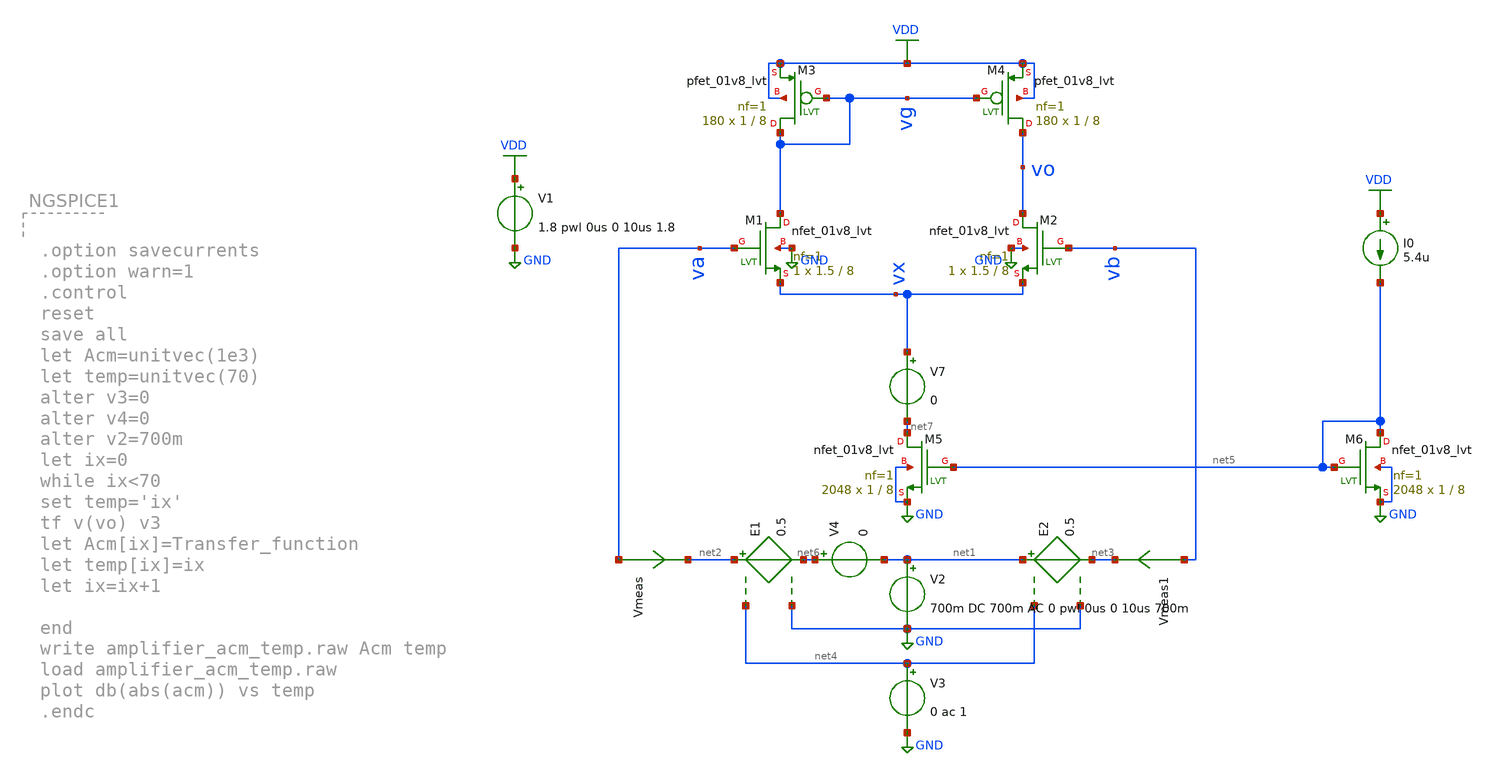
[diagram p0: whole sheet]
** sch_path: schematics/amplifier.sch
**.subckt amplifier
V1 VDD GND 1.8 pwl 0us 0 10us 1.8
V2 net1 GND 700m DC 700m AC 0 pwl 0us 0 10us 700m
Vmeas va net2 0
.save i(vmeas)
Vmeas1 vb net3 0
.save i(vmeas1)
XM2 vo vb vx GND sky130_fd_pr__nfet_01v8_lvt L=8 W=1.5 nf=1 ad='int((nf+1)/2) * W/nf * 0.29' as='int((nf+2)/2) * W/nf * 0.29'
+ pd='2*int((nf+1)/2) * (W/nf + 0.29)' ps='2*int((nf+2)/2) * (W/nf + 0.29)' nrd='0.29 / W' nrs='0.29 / W'
+ sa=0 sb=0 sd=0 mult=1 m=1
E1 net2 net6 net4 GND 0.5
E2 net1 net3 net4 GND 0.5
V3 net4 GND 0 ac 1
XM5 net7 net5 GND GND sky130_fd_pr__nfet_01v8_lvt L=8 W=1 nf=1 ad='int((nf+1)/2) * W/nf * 0.29' as='int((nf+2)/2) * W/nf * 0.29'
+ pd='2*int((nf+1)/2) * (W/nf + 0.29)' ps='2*int((nf+2)/2) * (W/nf + 0.29)' nrd='0.29 / W' nrs='0.29 / W'
+ sa=0 sb=0 sd=0 mult=2048 m=2048
XM6 net5 net5 GND GND sky130_fd_pr__nfet_01v8_lvt L=8 W=1 nf=1 ad='int((nf+1)/2) * W/nf * 0.29' as='int((nf+2)/2) * W/nf * 0.29'
+ pd='2*int((nf+1)/2) * (W/nf + 0.29)' ps='2*int((nf+2)/2) * (W/nf + 0.29)' nrd='0.29 / W' nrs='0.29 / W'
+ sa=0 sb=0 sd=0 mult=2048 m=2048
V4 net6 net1 0
XM1 vg va vx GND sky130_fd_pr__nfet_01v8_lvt L=8 W=1.5 nf=1 ad='int((nf+1)/2) * W/nf * 0.29' as='int((nf+2)/2) * W/nf * 0.29'
+ pd='2*int((nf+1)/2) * (W/nf + 0.29)' ps='2*int((nf+2)/2) * (W/nf + 0.29)' nrd='0.29 / W' nrs='0.29 / W'
+ sa=0 sb=0 sd=0 mult=1 m=1
XM3 vg vg VDD VDD sky130_fd_pr__pfet_01v8_lvt L=8 W=1 nf=1 ad='int((nf+1)/2) * W/nf * 0.29' as='int((nf+2)/2) * W/nf * 0.29'
+ pd='2*int((nf+1)/2) * (W/nf + 0.29)' ps='2*int((nf+2)/2) * (W/nf + 0.29)' nrd='0.29 / W' nrs='0.29 / W'
+ sa=0 sb=0 sd=0 mult=180 m=180
XM4 vo vg VDD VDD sky130_fd_pr__pfet_01v8_lvt L=8 W=1 nf=1 ad='int((nf+1)/2) * W/nf * 0.29' as='int((nf+2)/2) * W/nf * 0.29'
+ pd='2*int((nf+1)/2) * (W/nf + 0.29)' ps='2*int((nf+2)/2) * (W/nf + 0.29)' nrd='0.29 / W' nrs='0.29 / W'
+ sa=0 sb=0 sd=0 mult=180 m=180
V7 vx net7 0
I0 VDD net5 5.4u
**** begin user architecture code


.option savecurrents
.option warn=1

.control

save all   @m.xm1.msky130_fd_pr__nfet_01v8_lvt[id]  @m.xm2.msky130_fd_pr__nfet_01v8_lvt[id]
let Adm=unitvec(1e3)
let Vcm=unitvec(1e3)
let id1=unitvec(1e3)
let id2=unitvec(1e3)
let ix=0
alter v3=0
alter v4=0
while ix<1e3
let vcmtemp=ix/1e3
alter v2=vcmtemp
tf v(vo) v3
let Adm[ix]=Transfer_function
let Vcm[ix]=vcmtemp
let ix=ix+1
end
write amplifier_adm_vs_vcm.raw Adm Vcm
load amplifier_adm_vs_vcm.raw
plot (abs(adm)) vs vcm

op
let gm4=@m.xm4.msky130_fd_pr__pfet_01v8['gm']
let gm2=@m.xm2.msky130_fd_pr__nfet_01v8['gm']
let ib=@i0[current]
let irhs=@m.xm2.msky130_fd_pr__nfet_01v8['id']
let ilhs=@m.xm1.msky130_fd_pr__nfet_01v8['id']
let vthp=@m.xm3.msky130_fd_pr__pfet_01v8['vth']
let vthn=@m.xm1.msky130_fd_pr__nfet_01v8['vth']
print gm2 gm4
print irhs ilhs
let K=10^(-3.89062)
echo 'saturation cond. for M1 & M2 (by symmetry)'
echo 'is'
print vo - vx
echo 'greater than'
print vb - vx - vthn
echo 'saturation cond. for M3 & M4 (by symmetry)'
echo 'is'
print vdd - vo
echo 'greater than'
print vdd - vg - vthp
echo 'saturation cond. check w/ vo'
echo 'is'
print vo
echo 'between'
print vg + vthp
echo 'and'
print vb - vthn
echo 'common mode input sweep'
dc v2 -1.8 1.8 0.1
let vic=(va+vb)/2
let irhs=@m.xm2.msky130_fd_pr__nfet_01v8['id']
let ilhs=@m.xm1.msky130_fd_pr__nfet_01v8['id']
plot irhs ilhs ilhs/irhs
echo 'ac analysis'
ac dec 100 1 100e9
let vid=net2-net3
let irhs=@m.xm2.msky130_fd_pr__nfet_01v8['id']
let ilhs=@m.xm1.msky130_fd_pr__nfet_01v8['id']
plot db(abs(vo/vid))
echo 'dc gain (dB)'
print db(abs(vo/vid))[0]

dc i0 10u 100u 5u

.endc



.include $::SKYWATER_MODELS/cells/nfet_01v8/sky130_fd_pr__nfet_01v8__tt.corner.spice
.include $::SKYWATER_MODELS/cells/nfet_01v8_lvt/sky130_fd_pr__nfet_01v8_lvt__tt.corner.spice
.include $::SKYWATER_MODELS/cells/pfet_01v8/sky130_fd_pr__pfet_01v8__tt.corner.spice
.include $::SKYWATER_MODELS/cells/nfet_03v3_nvt/sky130_fd_pr__nfet_03v3_nvt__tt.corner.spice
.include $::SKYWATER_MODELS/cells/nfet_05v0_nvt/sky130_fd_pr__nfet_05v0_nvt__tt.corner.spice
.include $::SKYWATER_MODELS/cells/esd_nfet_01v8/sky130_fd_pr__esd_nfet_01v8__tt.corner.spice
.include $::SKYWATER_MODELS/cells/pfet_01v8_lvt/sky130_fd_pr__pfet_01v8_lvt__tt.corner.spice
.include $::SKYWATER_MODELS/cells/pfet_01v8_hvt/sky130_fd_pr__pfet_01v8_hvt__tt.corner.spice
.include $::SKYWATER_MODELS/cells/esd_pfet_g5v0d10v5/sky130_fd_pr__esd_pfet_g5v0d10v5__tt.corner.spice
.include $::SKYWATER_MODELS/cells/pfet_g5v0d10v5/sky130_fd_pr__pfet_g5v0d10v5__tt.corner.spice
.include $::SKYWATER_MODELS/cells/pfet_g5v0d16v0/sky130_fd_pr__pfet_g5v0d16v0__tt.corner.spice
.include $::SKYWATER_MODELS/cells/nfet_g5v0d10v5/sky130_fd_pr__nfet_g5v0d10v5__tt.corner.spice
.include $::SKYWATER_MODELS/cells/nfet_g5v0d16v0/sky130_fd_pr__nfet_g5v0d16v0__tt_discrete.corner.spice
.include $::SKYWATER_MODELS/cells/esd_nfet_g5v0d10v5/sky130_fd_pr__esd_nfet_g5v0d10v5__tt.corner.spice
.include $::SKYWATER_MODELS/models/corners/tt/nonfet.spice
* Mismatch parameters
.include $::SKYWATER_MODELS/cells/nfet_01v8/sky130_fd_pr__nfet_01v8__mismatch.corner.spice
.include $::SKYWATER_MODELS/cells/pfet_01v8/sky130_fd_pr__pfet_01v8__mismatch.corner.spice
.include $::SKYWATER_MODELS/cells/nfet_01v8_lvt/sky130_fd_pr__nfet_01v8_lvt__mismatch.corner.spice
.include $::SKYWATER_MODELS/cells/pfet_01v8_lvt/sky130_fd_pr__pfet_01v8_lvt__mismatch.corner.spice
.include $::SKYWATER_MODELS/cells/pfet_01v8_hvt/sky130_fd_pr__pfet_01v8_hvt__mismatch.corner.spice
.include $::SKYWATER_MODELS/cells/nfet_g5v0d10v5/sky130_fd_pr__nfet_g5v0d10v5__mismatch.corner.spice
.include $::SKYWATER_MODELS/cells/pfet_g5v0d10v5/sky130_fd_pr__pfet_g5v0d10v5__mismatch.corner.spice
.include $::SKYWATER_MODELS/cells/nfet_05v0_nvt/sky130_fd_pr__nfet_05v0_nvt__mismatch.corner.spice
.include $::SKYWATER_MODELS/cells/nfet_03v3_nvt/sky130_fd_pr__nfet_03v3_nvt__mismatch.corner.spice
* Resistor$::SKYWATER_MODELS/Capacitor
.include $::SKYWATER_MODELS/models/r+c/res_typical__cap_typical.spice
.include $::SKYWATER_MODELS/models/r+c/res_typical__cap_typical__lin.spice
* Special cells
.include $::SKYWATER_MODELS/models/corners/tt/specialized_cells.spice
* All models
.include $::SKYWATER_MODELS/models/all.spice
.include $::SKYWATER_MODELS/cells/pnp_05v5/sky130_fd_pr__pnp_05v5_W3p40L3p40.model.spice
* Corner
.include $::SKYWATER_MODELS/models/corners/tt/rf.spice

**** end user architecture code
**.ends
.GLOBAL GND
.GLOBAL VDD
.end
